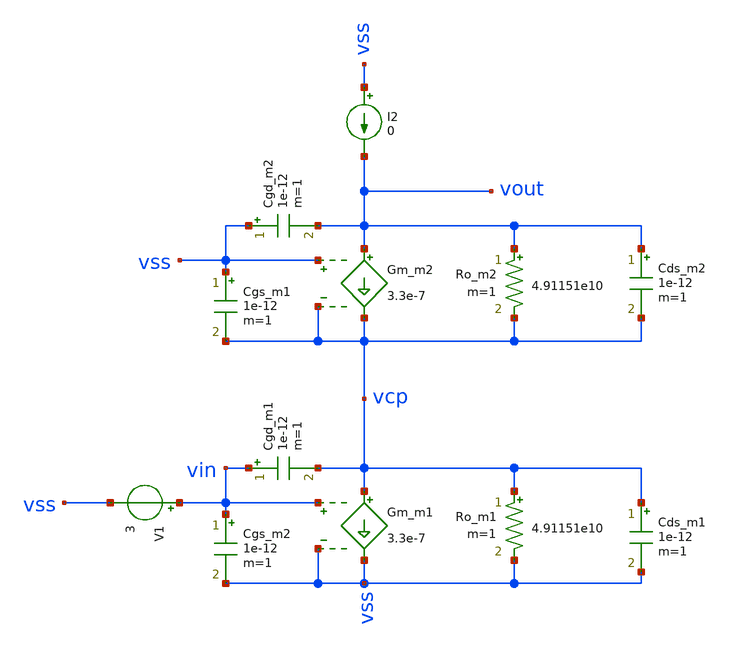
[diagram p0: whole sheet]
** sch_path: test-python/sstadex/xschem/cascode_test.sch
**.subckt cascode_test
Ro_m2 vout vcp 4.91151e10 m=1
Gm_m2 vout vcp vss vcp 3.3e-7
Cgd_m2 vss vout 1e-12 m=1
Cgs_m1 vss vcp 1e-12 m=1
Ro_m1 vcp vss 4.91151e10 m=1
Gm_m1 vcp vss vin vss 3.3e-7
Cgd_m1 vin vcp 1e-12 m=1
Cgs_m2 vin vss 1e-12 m=1
I2 vss vout 0
V1 vin vss 3
Cds_m2 vout vcp 1e-12 m=1
Cds_m1 vcp vss 1e-12 m=1
**.ends
.end
